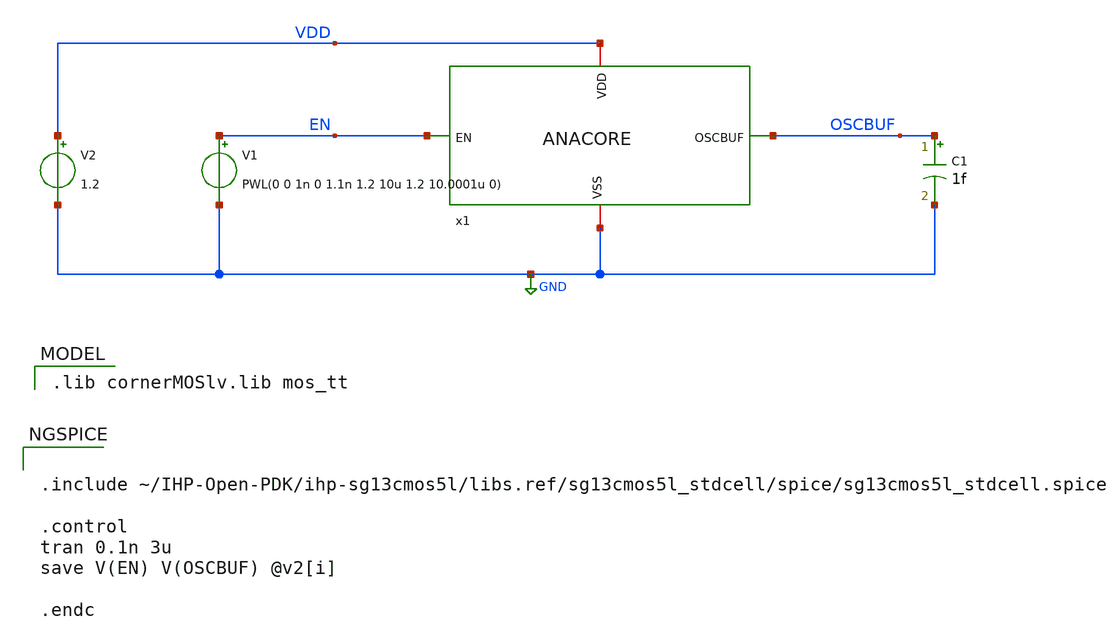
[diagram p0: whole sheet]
** sch_path: MPU9547-main/analog/schematic/tb_ANACORE_tran.sch
**.subckt tb_ANACORE_tran
x1 VDD EN OSCBUF GND ANACORE
V1 EN GND PWL(0 0 1n 0 1.1n 1.2 10u 1.2 10.0001u 0)
V2 VDD GND 1.2
C1 OSCBUF GND 1f m=1
**** begin user architecture code
 .lib cornerMOSlv.lib mos_tt



.include ~/IHP-Open-PDK/ihp-sg13cmos5l/libs.ref/sg13cmos5l_stdcell/spice/sg13cmos5l_stdcell.spice

.control
tran 0.1n 3u
save V(EN) V(OSCBUF) @v2[i]

.endc


**** end user architecture code
**.ends
.GLOBAL GND
.end
